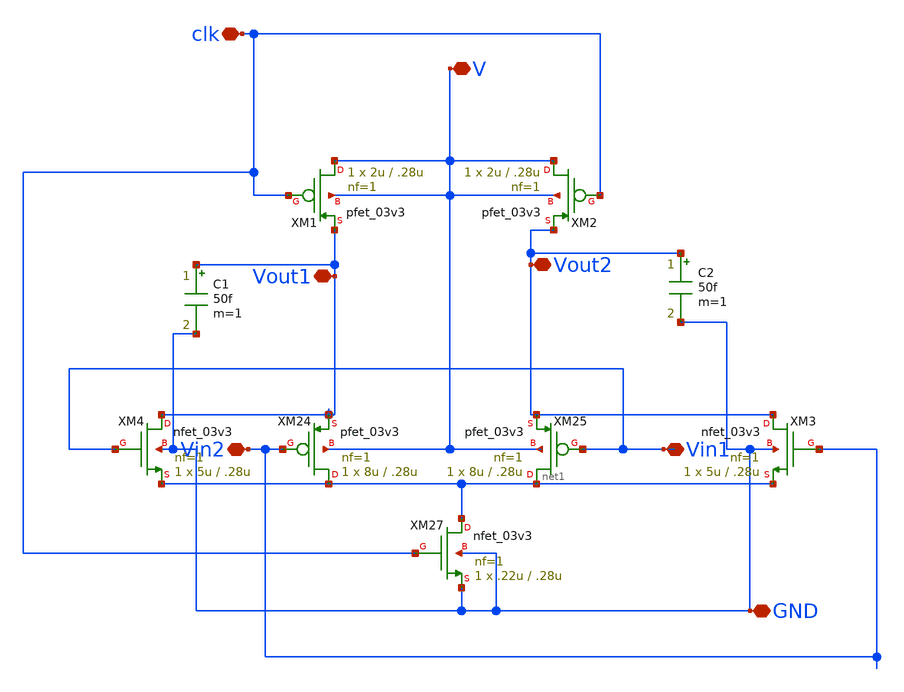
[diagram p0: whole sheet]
** sch_path: xschem/designs/preamp.sch
**.subckt preamp V GND Vout2 Vout1 clk Vin2 Vin1
*.iopin V
*.iopin GND
*.iopin Vout2
*.iopin Vout1
*.iopin clk
*.iopin Vin2
*.iopin Vin1
XM27 net1 clk GND GND nfet_03v3 L=.28u W=.22u nf=1 ad='int((nf+1)/2) * W/nf * 0.18u' as='int((nf+2)/2) * W/nf * 0.18u'
+ pd='2*int((nf+1)/2) * (W/nf + 0.18u)' ps='2*int((nf+2)/2) * (W/nf + 0.18u)' nrd='0.18u / W' nrs='0.18u / W'
+ sa=0 sb=0 sd=0 m=1
XM24 net1 Vin2 Vout1 V pfet_03v3 L=.28u W=8u nf=1 ad='int((nf+1)/2) * W/nf * 0.18u' as='int((nf+2)/2) * W/nf * 0.18u'
+ pd='2*int((nf+1)/2) * (W/nf + 0.18u)' ps='2*int((nf+2)/2) * (W/nf + 0.18u)' nrd='0.18u / W' nrs='0.18u / W'
+ sa=0 sb=0 sd=0 m=1
XM25 net1 Vin1 Vout2 V pfet_03v3 L=.28u W=8u nf=1 ad='int((nf+1)/2) * W/nf * 0.18u' as='int((nf+2)/2) * W/nf * 0.18u'
+ pd='2*int((nf+1)/2) * (W/nf + 0.18u)' ps='2*int((nf+2)/2) * (W/nf + 0.18u)' nrd='0.18u / W' nrs='0.18u / W'
+ sa=0 sb=0 sd=0 m=1
XM1 V clk Vout1 V pfet_03v3 L=.28u W=2u nf=1 ad='int((nf+1)/2) * W/nf * 0.18u' as='int((nf+2)/2) * W/nf * 0.18u'
+ pd='2*int((nf+1)/2) * (W/nf + 0.18u)' ps='2*int((nf+2)/2) * (W/nf + 0.18u)' nrd='0.18u / W' nrs='0.18u / W'
+ sa=0 sb=0 sd=0 m=1
XM2 V clk Vout2 V pfet_03v3 L=.28u W=2u nf=1 ad='int((nf+1)/2) * W/nf * 0.18u' as='int((nf+2)/2) * W/nf * 0.18u'
+ pd='2*int((nf+1)/2) * (W/nf + 0.18u)' ps='2*int((nf+2)/2) * (W/nf + 0.18u)' nrd='0.18u / W' nrs='0.18u / W'
+ sa=0 sb=0 sd=0 m=1
XM3 Vout2 Vin2 net1 GND nfet_03v3 L=.28u W=5u nf=1 ad='int((nf+1)/2) * W/nf * 0.18u' as='int((nf+2)/2) * W/nf * 0.18u'
+ pd='2*int((nf+1)/2) * (W/nf + 0.18u)' ps='2*int((nf+2)/2) * (W/nf + 0.18u)' nrd='0.18u / W' nrs='0.18u / W'
+ sa=0 sb=0 sd=0 m=1
XM4 Vout1 Vin1 net1 GND nfet_03v3 L=.28u W=5u nf=1 ad='int((nf+1)/2) * W/nf * 0.18u' as='int((nf+2)/2) * W/nf * 0.18u'
+ pd='2*int((nf+1)/2) * (W/nf + 0.18u)' ps='2*int((nf+2)/2) * (W/nf + 0.18u)' nrd='0.18u / W' nrs='0.18u / W'
+ sa=0 sb=0 sd=0 m=1
C1 Vout1 GND 50f m=1
C2 Vout2 GND 50f m=1
**.ends
.end
